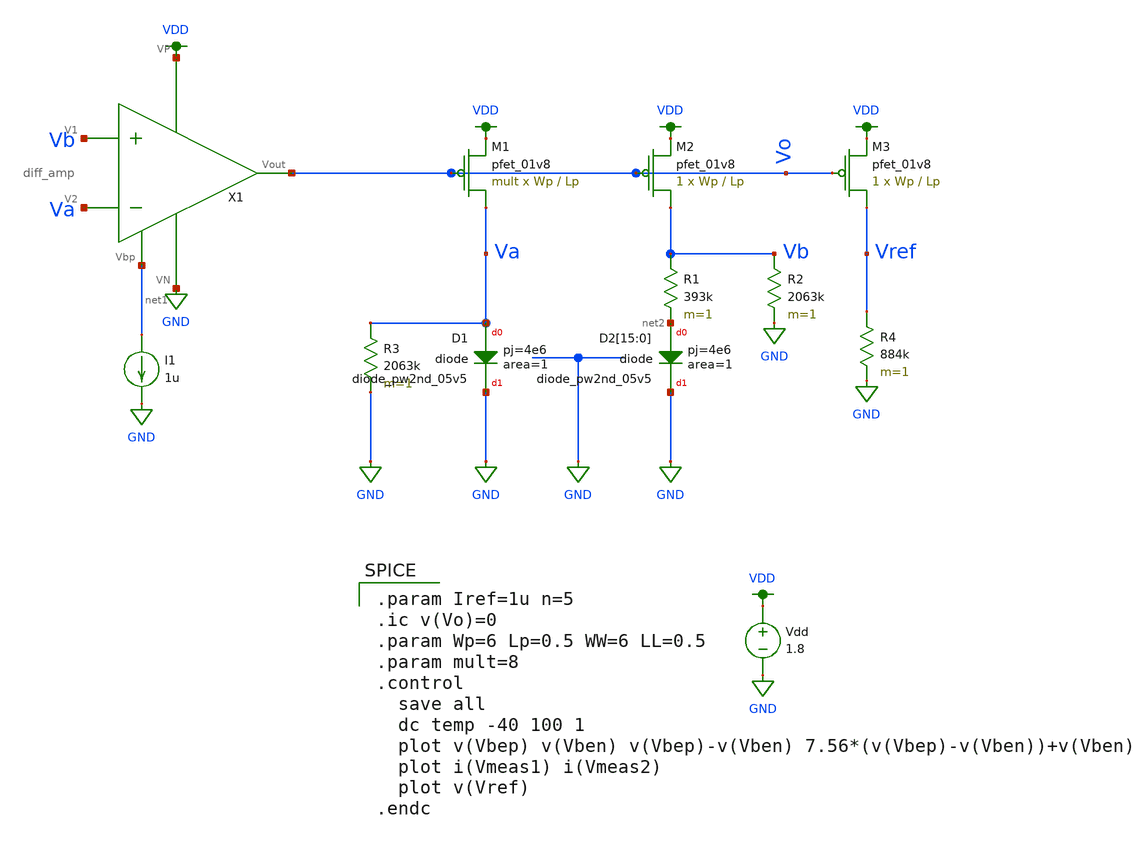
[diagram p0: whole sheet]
** sch_path: schematic/test/archive/bandgap_lv.sch
**.subckt bandgap_lv
Vdd VDD GND 1.8
XM1 Va Vo VDD VDD sky130_fd_pr__pfet_01v8 L=Lp W=Wp nf=1 ad='int((nf+1)/2) * W/nf * 0.29' as='int((nf+2)/2) * W/nf * 0.29'
+ pd='2*int((nf+1)/2) * (W/nf + 0.29)' ps='2*int((nf+2)/2) * (W/nf + 0.29)' nrd='0.29 / W' nrs='0.29 / W'
+ sa=0 sb=0 sd=0 mult=mult m=mult
XM2 Vb Vo VDD VDD sky130_fd_pr__pfet_01v8 L=Lp W=Wp nf=1 ad='int((nf+1)/2) * W/nf * 0.29' as='int((nf+2)/2) * W/nf * 0.29'
+ pd='2*int((nf+1)/2) * (W/nf + 0.29)' ps='2*int((nf+2)/2) * (W/nf + 0.29)' nrd='0.29 / W' nrs='0.29 / W'
+ sa=0 sb=0 sd=0 mult=1 m=1
R4 Vref GND 884k m=1
XM3 Vref Vo VDD VDD sky130_fd_pr__pfet_01v8 L=Lp W=Wp nf=1 ad='int((nf+1)/2) * W/nf * 0.29' as='int((nf+2)/2) * W/nf * 0.29'
+ pd='2*int((nf+1)/2) * (W/nf + 0.29)' ps='2*int((nf+2)/2) * (W/nf + 0.29)' nrd='0.29 / W' nrs='0.29 / W'
+ sa=0 sb=0 sd=0 mult=1 m=1
R1 Vb net2 393k m=1
R2 Vb GND 2063k m=1
R3 Va GND 2063k m=1
X1 VDD net1 Vo Vb Va GND diff_amp
I1 net1 GND 1u
XD1 Va GND sky130_fd_pr__diode_pw2nd_05v5 area=1 pj=4e6
XD2[15] net2 GND sky130_fd_pr__diode_pw2nd_05v5 area=1 pj=4e6
XD2[14] net2 GND sky130_fd_pr__diode_pw2nd_05v5 area=1 pj=4e6
XD2[13] net2 GND sky130_fd_pr__diode_pw2nd_05v5 area=1 pj=4e6
XD2[12] net2 GND sky130_fd_pr__diode_pw2nd_05v5 area=1 pj=4e6
XD2[11] net2 GND sky130_fd_pr__diode_pw2nd_05v5 area=1 pj=4e6
XD2[10] net2 GND sky130_fd_pr__diode_pw2nd_05v5 area=1 pj=4e6
XD2[9] net2 GND sky130_fd_pr__diode_pw2nd_05v5 area=1 pj=4e6
XD2[8] net2 GND sky130_fd_pr__diode_pw2nd_05v5 area=1 pj=4e6
XD2[7] net2 GND sky130_fd_pr__diode_pw2nd_05v5 area=1 pj=4e6
XD2[6] net2 GND sky130_fd_pr__diode_pw2nd_05v5 area=1 pj=4e6
XD2[5] net2 GND sky130_fd_pr__diode_pw2nd_05v5 area=1 pj=4e6
XD2[4] net2 GND sky130_fd_pr__diode_pw2nd_05v5 area=1 pj=4e6
XD2[3] net2 GND sky130_fd_pr__diode_pw2nd_05v5 area=1 pj=4e6
XD2[2] net2 GND sky130_fd_pr__diode_pw2nd_05v5 area=1 pj=4e6
XD2[1] net2 GND sky130_fd_pr__diode_pw2nd_05v5 area=1 pj=4e6
XD2[0] net2 GND sky130_fd_pr__diode_pw2nd_05v5 area=1 pj=4e6
**** begin user architecture code

.option wnflag=1
.param MC_SWITCH=0.0
.lib /media/qdeng/526448C32060CF5C/skywater/skywater-pdk/libraries/sky130_fd_pr_ngspice/latest/models/sky130.lib.spice tt


.param Iref=1u n=5
.ic v(Vo)=0
.param Wp=6 Lp=0.5 WW=6 LL=0.5
.param mult=8
.control
  save all
  dc temp -40 100 1
  plot v(Vbep) v(Vben) v(Vbep)-v(Vben) 7.56*(v(Vbep)-v(Vben))+v(Vben)
  plot i(Vmeas1) i(Vmeas2)
  plot v(Vref)
.endc

**** end user architecture code
**.ends
.GLOBAL GND
.GLOBAL VDD
.end
